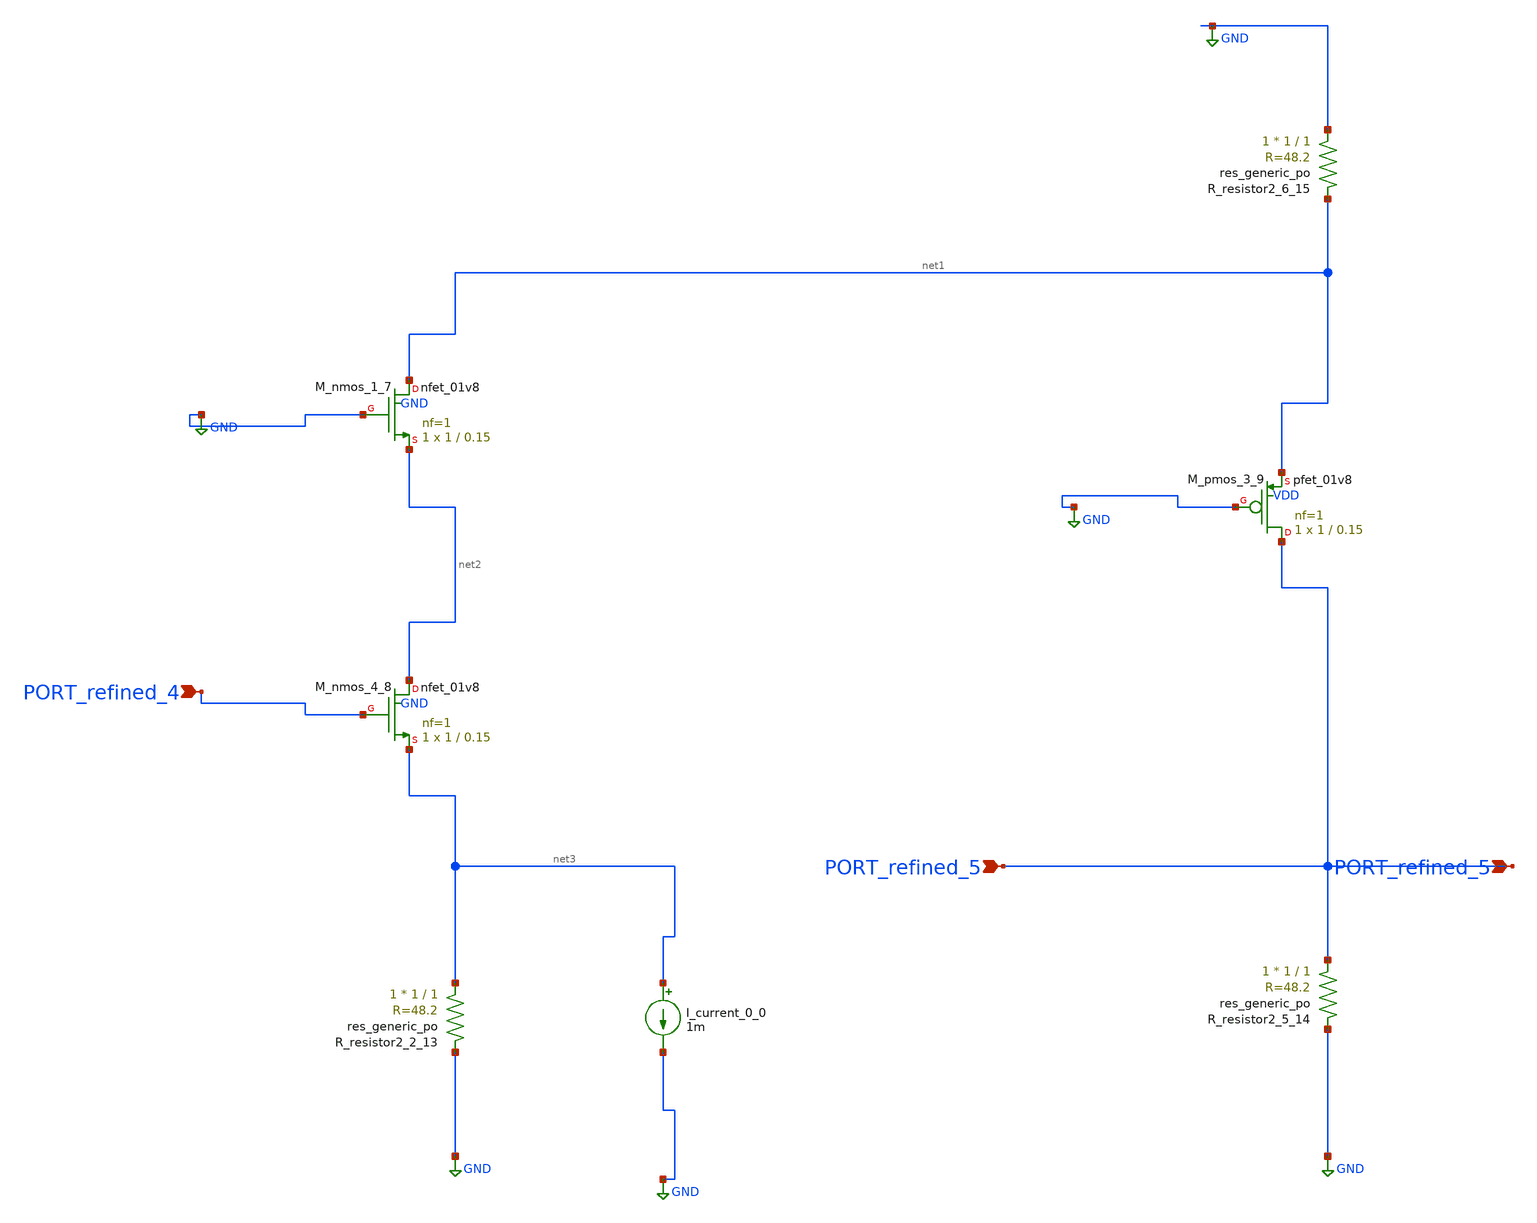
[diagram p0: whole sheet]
** sch_path: schematics/AMSNet/670.sch
**.subckt 670 PORT_refined_4 PORT_refined_5 PORT_refined_5
*.ipin PORT_refined_4
*.ipin PORT_refined_5
*.ipin PORT_refined_5
I_current_0_0 net3 GND 1m
XM_nmos_1_7 net1 GND net2 GND sky130_fd_pr__nfet_01v8 L=0.15 W=1 nf=1 ad='int((1 + 1)/2) * 1 / 1 * 0.29'
+ as='int((1 + 2)/2) * 1 / 1 * 0.29' pd='2*int((1 + 1)/2) * (1 / 1 + 0.29)' ps='2*int((1 + 2)/2) * (1 / 1 + 0.29)'
+ nrd='0.29 / 1 ' nrs='0.29 / 1 ' sa=0 sb=0 sd=0 mult=1 m=1
XM_nmos_4_8 net2 PORT_refined_4 net3 GND sky130_fd_pr__nfet_01v8 L=0.15 W=1 nf=1 ad='int((1 + 1)/2) * 1 / 1 * 0.29'
+ as='int((1 + 2)/2) * 1 / 1 * 0.29' pd='2*int((1 + 1)/2) * (1 / 1 + 0.29)' ps='2*int((1 + 2)/2) * (1 / 1 + 0.29)'
+ nrd='0.29 / 1 ' nrs='0.29 / 1 ' sa=0 sb=0 sd=0 mult=1 m=1
XM_pmos_3_9 PORT_refined_5 GND net1 VDD sky130_fd_pr__pfet_01v8 L=0.15 W=1 nf=1 ad='int((1 + 1)/2) * 1 / 1 * 0.29'
+ as='int((1 + 2)/2) * 1 / 1 * 0.29' pd='2*int((1 + 1)/2) * (1 / 1 + 0.29)' ps='2*int((1 + 2)/2) * (1 / 1 + 0.29)'
+ nrd='0.29 / 1 ' nrs='0.29 / 1 ' sa=0 sb=0 sd=0 mult=1 m=1
XR_resistor2_2_13 net3 GND sky130_fd_pr__res_generic_po W=1 L=1 m=1
XR_resistor2_5_14 PORT_refined_5 GND sky130_fd_pr__res_generic_po W=1 L=1 m=1
XR_resistor2_6_15 GND net1 sky130_fd_pr__res_generic_po W=1 L=1 m=1
**.ends
.GLOBAL GND
.end
